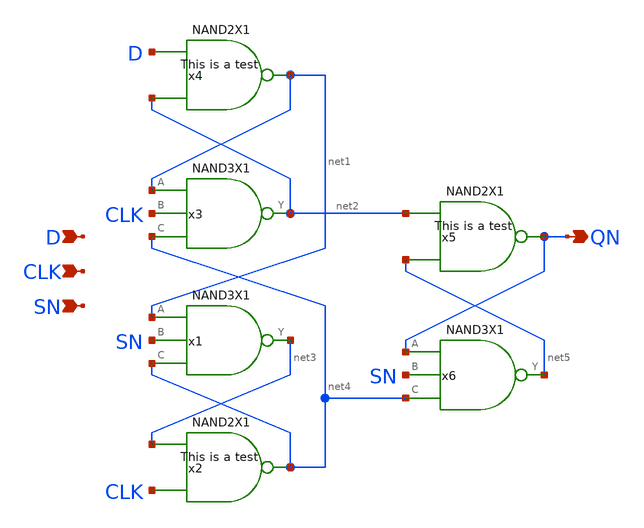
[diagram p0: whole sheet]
** sch_path: archives/lib/xschem/DFFSNQNX1.sch
**.subckt DFFSNQNX1 QN D CLK SN
*.opin QN
*.ipin D
*.ipin CLK
*.ipin SN
x1 net3 net1 SN net4 VDD VSS NAND3X1
x2 net4 net3 CLK VDD VSS NAND2X1
x3 net2 net1 CLK net4 VDD VSS NAND3X1
x4 net1 D net2 VDD VSS NAND2X1
x5 QN net2 net5 VDD VSS NAND2X1
x6 net5 QN SN net4 VDD VSS NAND3X1
**.ends
.end
